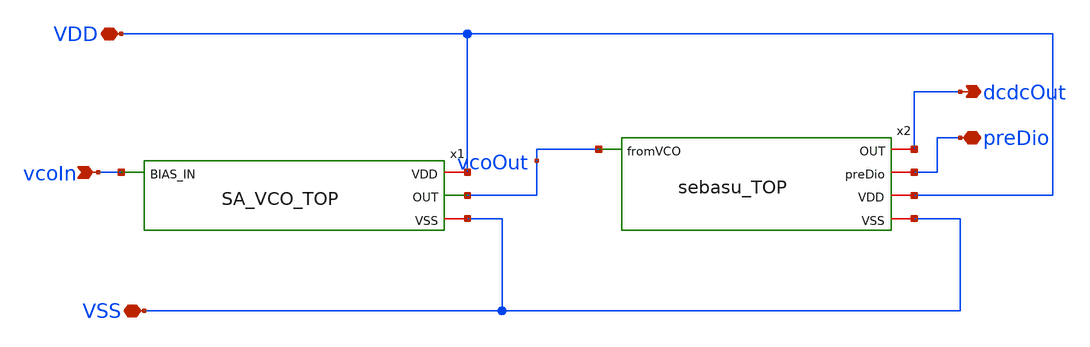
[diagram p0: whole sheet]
** sch_path: design/xschem/SA_sebasu_TOP.sch
**.subckt SA_sebasu_TOP vcoIn VSS VDD preDio dcdcOut
*.ipin vcoIn
*.iopin VSS
*.iopin VDD
*.iopin preDio
*.opin dcdcOut
x1 VDD vcoIn vcoOut VSS SA_VCO_TOP
x2 dcdcOut preDio VDD vcoOut VSS sebasu_TOP
**.ends
.end
